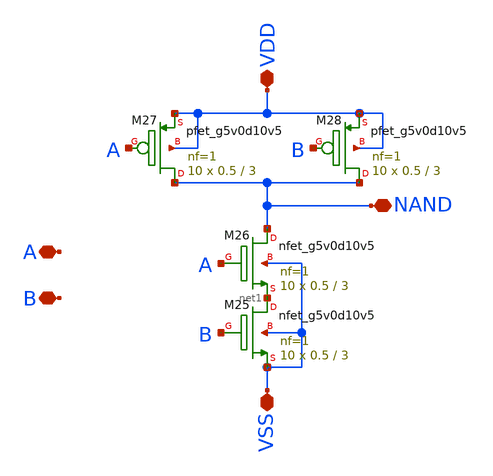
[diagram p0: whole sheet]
** sch_path: xschem/nand_5v.sch
**.subckt nand_5v VSS VDD A B NAND
*.iopin VSS
*.iopin VDD
*.iopin A
*.iopin B
*.iopin NAND
XM25 net1 B VSS VSS sky130_fd_pr__nfet_g5v0d10v5 L=3 W=0.5 nf=1 ad='int((nf+1)/2) * W/nf * 0.29' as='int((nf+2)/2) * W/nf * 0.29'
+ pd='2*int((nf+1)/2) * (W/nf + 0.29)' ps='2*int((nf+2)/2) * (W/nf + 0.29)' nrd='0.29 / W' nrs='0.29 / W'
+ sa=0 sb=0 sd=0 mult=10 m=10
XM26 NAND A net1 VSS sky130_fd_pr__nfet_g5v0d10v5 L=3 W=0.5 nf=1 ad='int((nf+1)/2) * W/nf * 0.29' as='int((nf+2)/2) * W/nf * 0.29'
+ pd='2*int((nf+1)/2) * (W/nf + 0.29)' ps='2*int((nf+2)/2) * (W/nf + 0.29)' nrd='0.29 / W' nrs='0.29 / W'
+ sa=0 sb=0 sd=0 mult=10 m=10
XM27 NAND A VDD VDD sky130_fd_pr__pfet_g5v0d10v5 L=3 W=0.5 nf=1 ad='int((nf+1)/2) * W/nf * 0.29' as='int((nf+2)/2) * W/nf * 0.29'
+ pd='2*int((nf+1)/2) * (W/nf + 0.29)' ps='2*int((nf+2)/2) * (W/nf + 0.29)' nrd='0.29 / W' nrs='0.29 / W'
+ sa=0 sb=0 sd=0 mult=10 m=10
XM28 NAND B VDD VDD sky130_fd_pr__pfet_g5v0d10v5 L=3 W=0.5 nf=1 ad='int((nf+1)/2) * W/nf * 0.29' as='int((nf+2)/2) * W/nf * 0.29'
+ pd='2*int((nf+1)/2) * (W/nf + 0.29)' ps='2*int((nf+2)/2) * (W/nf + 0.29)' nrd='0.29 / W' nrs='0.29 / W'
+ sa=0 sb=0 sd=0 mult=10 m=10
**.ends
.end
